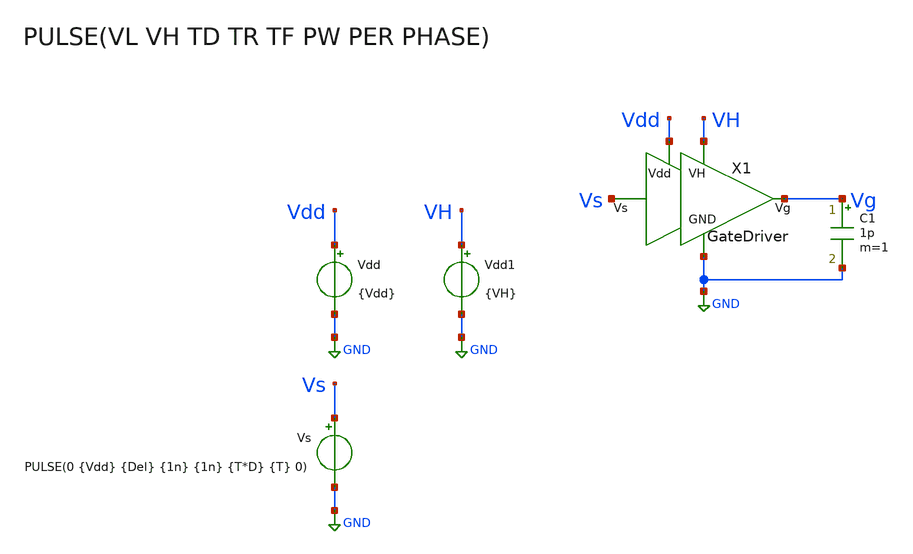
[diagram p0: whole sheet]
** sch_path: ChipUSM_AnalogTrack24/GD/TB_GateDriver.sch
**.subckt TB_GateDriver
X1 Vs Vg Vdd VH GND GateDriver
Vdd Vdd GND {Vdd}
Vs Vs GND PULSE(0 {Vdd} {Del} {1n} {1n} {T*D} {T} 0)
Vdd1 VH GND {VH}
C1 Vg GND 1p m=1
**** begin user architecture code

.lib cornerMOShv.lib mos_tt
.lib cornerMOSlv.lib mos_tt



.param Vdd = 1.2
.param VH = 3.3

.param D = 0.5
*.param T = 1u
.param T = 0.1u
.param TR = 10n
.param TF = 10n
*.param TdR = 0.1u
.param TdR = 1n
*.param TdF = 0.1u
.param TdF = 1n
.param Del = 0.05u
.param temp = 27






.save all
.control
reset
set color0 = white
tran 1n 1u
plot v(Vs)
plot v(Vg)
plot v(x1.VgMD2)
plot v(x1.VgMD5)
plot v(x1.VgMD78)
*meas TRAN td_off_M1 TRIG v(Vg_M1) VAL=0.33 RISE=1 TARG VsdM1 VAL=0.33 RISE=1
*meas TRAN td_on_M1 TRIG v(Vg_M1) VAL=2.97 FALL=1 TARG VsdM1 VAL=2.97 FALL=1
*meas TRAN td_on_M2 TRIG v(Vg_M2) VAL=0.33 RISE=1 TARG VdsM2 VAL=2.97 FALL=1
*meas TRAN td_off_M2 TRIG v(Vg_M2) VAL=2.97 FALL=1 TARG VdsM2 VAL=0.33 RISE=1
*let TdR = td_off_M1 - td_on_M2
*let TdF = td_on_M1 - td_off_M2
*print TdR TdF
.endc

.end




.param temp=27

*.param mult_13 = 1
*.param mult_24 = 6
*.param mult_5 = 100
*.param mult_6 = 100
*.param mult_7 = 200
*.param mult_8 = 200
*.param mult_9 = 5
*.param mult_10 = 5

.param mult_13 = 1
.param mult_24 = 10
.param mult_5 = 20
.param mult_6 = 20
.param mult_7 = 40
.param mult_8 = 40
.param mult_9 = 10
.param mult_10 = 10

.param ng_13 = 1
.param ng_24 = 1
.param ng_5 = 1
.param ng_6 = 1
.param ng_7 = 1
.param ng_8 = 1
.param ng_9 = 1
.param ng_10 = 1

.param l_1357 = 0.45u
.param w_1357 = 0.3u
.param l_2468 = 0.4u
.param w_2468 = 0.3u
.param l_9 = 0.13u
.param w_9 = 0.15u
.param l_10 = 0.13u
.param w_10 = 0.15u




**** end user architecture code
**.ends

* expanding   symbol:  GateDriver.sym # of pins=5
** sym_path: ChipUSM_AnalogTrack24/GD/GateDriver.sym
** sch_path: ChipUSM_AnalogTrack24/GD/GateDriver.sch
.subckt GateDriver Vs Vg Vdd VH GND
*.iopin VH
*.iopin Vdd
*.ipin Vs
*.opin Vg
*.iopin GND
XMD9 VgMD2 Vs Vdd Vdd sg13_lv_pmos w={w_9} l={l_9} ng={ng_9} m={mult_9} mm_ok=1
XMD10 GND Vs VgMD2 GND sg13_lv_nmos w={w_10} l={l_10} ng={ng_10} m={mult_10} mm_ok=1
XMD1 VgMD5 net1 VH VH sg13_hv_pmos w={w_1357} l={l_1357} ng={ng_13} m={mult_13} mm_ok=1
XMD3 net1 VgMD5 VH VH sg13_hv_pmos w={w_1357} l={l_1357} ng={ng_13} m={mult_13} mm_ok=1
XMD5 net2 VgMD5 VH VH sg13_hv_pmos w={w_1357} l={l_1357} ng={ng_5} m={mult_5} mm_ok=1
XMD7 Vg VgMd78 VH VH sg13_hv_pmos w={w_1357} l={l_1357} ng={ng_7} m={mult_7} mm_ok=1
XMD2 GND VgMD2 VgMD5 GND sg13_hv_nmos w={w_2468} l={l_2468} ng={ng_24} m={mult_24} mm_ok=1
XMD4 GND Vs net1 GND sg13_hv_nmos w={w_2468} l={l_2468} ng={ng_24} m={mult_24} mm_ok=1
XMD6 GND Vs net2 GND sg13_hv_nmos w={w_2468} l={l_2468} ng={ng_6} m={mult_6} mm_ok=1
XMD8 GND VgMd78 Vg GND sg13_hv_nmos w={w_2468} l={l_2468} ng={ng_8} m={mult_8} mm_ok=1
VIg78 net2 VgMd78 0
.save i(vig78)
.ends

.GLOBAL GND
.end
